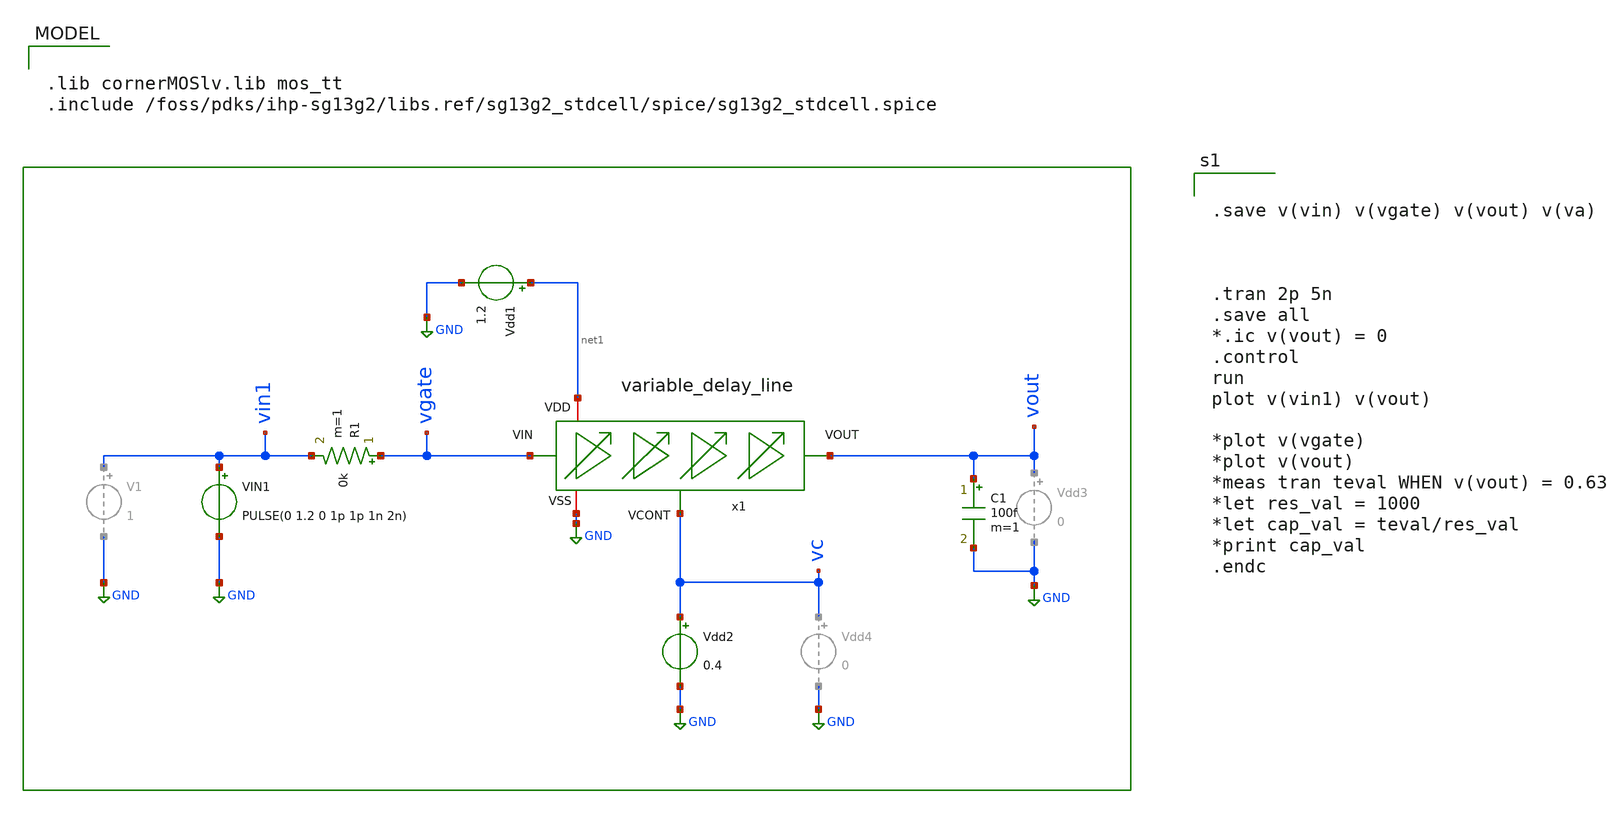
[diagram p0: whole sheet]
** sch_path: sch/delay_variable_line/tb_variable_delay_line.sch
**.subckt tb_variable_delay_line
x1 net1 GND vc net2 vgate variable_delay_line
R1 vgate vin1 0k m=1
Vdd1 net1 GND 1.2
Vdd2 vc GND 0.4
C1 vout GND 100f m=1
VIN1 vin1 GND PULSE(0 1.2 0 1p 1p 1n 2n)
**** begin user architecture code

.lib cornerMOSlv.lib mos_tt
.include /foss/pdks/ihp-sg13g2/libs.ref/sg13g2_stdcell/spice/sg13g2_stdcell.spice



.save v(vin) v(vgate) v(vout) v(va)



.tran 2p 5n
.save all
*.ic v(vout) = 0
.control
run
plot v(vin1) v(vout)

*plot v(vgate)
*plot v(vout)
*meas tran teval WHEN v(vout) = 0.63
*let res_val = 1000
*let cap_val = teval/res_val
*print cap_val
.endc


**** end user architecture code
**.ends

* expanding   symbol:  /foss/designs/DLL/variable_delay_line.sym # of pins=5
** sym_path: sch/delay_variable_line/variable_delay_line.sym
** sch_path: sch/delay_variable_line/variable_delay_line.sch
.subckt variable_delay_line VDD VSS VCONT VOUT VIN
*.iopin VSS
*.iopin VDD
*.ipin VIN
*.opin VOUT
*.ipin VCONT
x1 VDD VIN net1 VCONT VSS variable_delay
x2 VDD net1 net2 VCONT VSS variable_delay
x3 VDD net2 net5 VCONT VSS variable_delay
x4 VDD net5 net3 VCONT VSS variable_delay
x5 VDD net3 net4 VCONT VSS variable_delay
x6 VDD net4 VOUT VCONT VSS variable_delay
.ends


* expanding   symbol:  /foss/designs/DLL/variable_delay.sym # of pins=5
** sym_path: sch/delay_variable_line/variable_delay.sym
** sch_path: sch/delay_variable_line/variable_delay.sch
.subckt variable_delay VDD_D VIN_D VOUT_D VCONT_D VSS_D
*.iopin VSS_D
*.iopin VDD_D
*.ipin VIN_D
*.opin VOUT_D
*.ipin VCONT_D
XM3 net4 VCONT_D net2 net2 sg13_lv_nmos w=1u l=0.13u ng=1 m=1 mm_ok=1
XM5 net3 VCONT_D net2 net2 sg13_lv_nmos w=1u l=5u ng=1 m=1 mm_ok=1
XM4 net4 net4 VDD_D VDD_D sg13_lv_pmos w=1u l=0.13u ng=1 m=1 mm_ok=1
XM6 net1 net4 VDD_D VDD_D sg13_lv_pmos w=1u l=5u ng=1 m=1 mm_ok=1
XM2 VOUT_D VIN_D net1 VDD_D sg13_lv_pmos w=10u l=10u ng=1 m=1 mm_ok=1
XM1 VOUT_D VIN_D net3 net2 sg13_lv_nmos w=10u l=10u ng=1 m=1 mm_ok=1
.ends

.GLOBAL GND
.end
